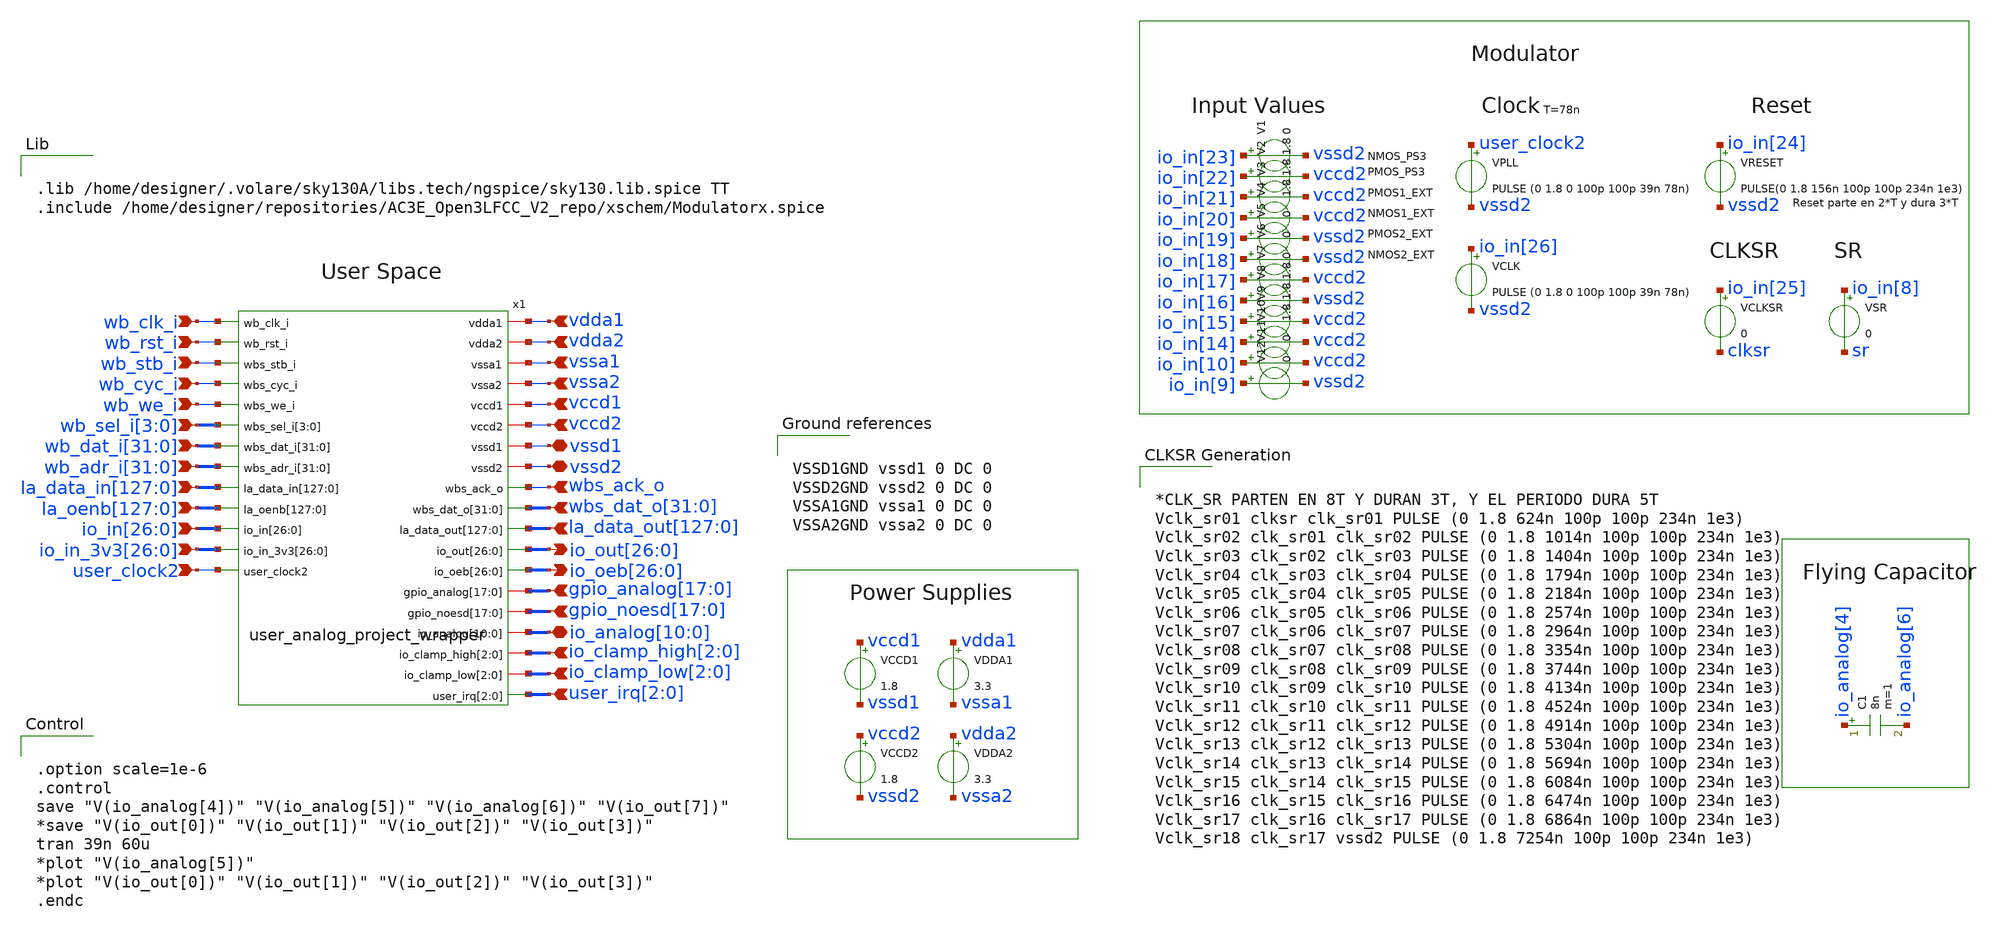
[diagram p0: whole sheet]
** sch_path: xschem/tb_top.sch
**.subckt tb_top vdda1 vdda2 vssa1 vssa2 vccd1 vccd2 vssd1 vssd2 wbs_ack_o
*+ wbs_dat_o[31],wbs_dat_o[30],wbs_dat_o[29],wbs_dat_o[28],wbs_dat_o[27],wbs_dat_o[26],wbs_dat_o[25],wbs_dat_o[24],wbs_dat_o[23],wbs_dat_o[22],wbs_dat_o[21],wbs_dat_o[20],wbs_dat_o[19],wbs_dat_o[18],wbs_dat_o[17],wbs_dat_o[16],wbs_dat_o[15],wbs_dat_o[14],wbs_dat_o[13],wbs_dat_o[12],wbs_dat_o[11],wbs_dat_o[10],wbs_dat_o[9],wbs_dat_o[8],wbs_dat_o[7],wbs_dat_o[6],wbs_dat_o[5],wbs_dat_o[4],wbs_dat_o[3],wbs_dat_o[2],wbs_dat_o[1],wbs_dat_o[0]
*+ la_data_out[127],la_data_out[126],la_data_out[125],la_data_out[124],la_data_out[123],la_data_out[122],la_data_out[121],la_data_out[120],la_data_out[119],la_data_out[118],la_data_out[117],la_data_out[116],la_data_out[115],la_data_out[114],la_data_out[113],la_data_out[112],la_data_out[111],la_data_out[110],la_data_out[109],la_data_out[108],la_data_out[107],la_data_out[106],la_data_out[105],la_data_out[104],la_data_out[103],la_data_out[102],la_data_out[101],la_data_out[100],la_data_out[99],la_data_out[98],la_data_out[97],la_data_out[96],la_data_out[95],la_data_out[94],la_data_out[93],la_data_out[92],la_data_out[91],la_data_out[90],la_data_out[89],la_data_out[88],la_data_out[87],la_data_out[86],la_data_out[85],la_data_out[84],la_data_out[83],la_data_out[82],la_data_out[81],la_data_out[80],la_data_out[79],la_data_out[78],la_data_out[77],la_data_out[76],la_data_out[75],la_data_out[74],la_data_out[73],la_data_out[72],la_data_out[71],la_data_out[70],la_data_out[69],la_data_out[68],la_data_out[67],la_data_out[66],la_data_out[65],la_data_out[64],la_data_out[63],la_data_out[62],la_data_out[61],la_data_out[60],la_data_out[59],la_data_out[58],la_data_out[57],la_data_out[56],la_data_out[55],la_data_out[54],la_data_out[53],la_data_out[52],la_data_out[51],la_data_out[50],la_data_out[49],la_data_out[48],la_data_out[47],la_data_out[46],la_data_out[45],la_data_out[44],la_data_out[43],la_data_out[42],la_data_out[41],la_data_out[40],la_data_out[39],la_data_out[38],la_data_out[37],la_data_out[36],la_data_out[35],la_data_out[34],la_data_out[33],la_data_out[32],la_data_out[31],la_data_out[30],la_data_out[29],la_data_out[28],la_data_out[27],la_data_out[26],la_data_out[25],la_data_out[24],la_data_out[23],la_data_out[22],la_data_out[21],la_data_out[20],la_data_out[19],la_data_out[18],la_data_out[17],la_data_out[16],la_data_out[15],la_data_out[14],la_data_out[13],la_data_out[12],la_data_out[11],la_data_out[10],la_data_out[9],la_data_out[8],la_data_out[7],la_data_out[6],la_data_out[5],la_data_out[4],la_data_out[3],la_data_out[2],la_data_out[1],la_data_out[0]
*+ io_out[26],io_out[25],io_out[24],io_out[23],io_out[22],io_out[21],io_out[20],io_out[19],io_out[18],io_out[17],io_out[16],io_out[15],io_out[14],io_out[13],io_out[12],io_out[11],io_out[10],io_out[9],io_out[8],io_out[7],io_out[6],io_out[5],io_out[4],io_out[3],io_out[2],io_out[1],io_out[0]
*+ io_oeb[26],io_oeb[25],io_oeb[24],io_oeb[23],io_oeb[22],io_oeb[21],io_oeb[20],io_oeb[19],io_oeb[18],io_oeb[17],io_oeb[16],io_oeb[15],io_oeb[14],io_oeb[13],io_oeb[12],io_oeb[11],io_oeb[10],io_oeb[9],io_oeb[8],io_oeb[7],io_oeb[6],io_oeb[5],io_oeb[4],io_oeb[3],io_oeb[2],io_oeb[1],io_oeb[0]
*+ gpio_analog[17],gpio_analog[16],gpio_analog[15],gpio_analog[14],gpio_analog[13],gpio_analog[12],gpio_analog[11],gpio_analog[10],gpio_analog[9],gpio_analog[8],gpio_analog[7],gpio_analog[6],gpio_analog[5],gpio_analog[4],gpio_analog[3],gpio_analog[2],gpio_analog[1],gpio_analog[0]
*+ gpio_noesd[17],gpio_noesd[16],gpio_noesd[15],gpio_noesd[14],gpio_noesd[13],gpio_noesd[12],gpio_noesd[11],gpio_noesd[10],gpio_noesd[9],gpio_noesd[8],gpio_noesd[7],gpio_noesd[6],gpio_noesd[5],gpio_noesd[4],gpio_noesd[3],gpio_noesd[2],gpio_noesd[1],gpio_noesd[0]
*+ io_analog[10],io_analog[9],io_analog[8],io_analog[7],io_analog[6],io_analog[5],io_analog[4],io_analog[3],io_analog[2],io_analog[1],io_analog[0] io_clamp_high[2],io_clamp_high[1],io_clamp_high[0] io_clamp_low[2],io_clamp_low[1],io_clamp_low[0]
*+ user_irq[2],user_irq[1],user_irq[0] wb_clk_i wb_rst_i wb_stb_i wb_cyc_i wb_we_i wb_sel_i[3],wb_sel_i[2],wb_sel_i[1],wb_sel_i[0]
*+ wb_dat_i[31],wb_dat_i[30],wb_dat_i[29],wb_dat_i[28],wb_dat_i[27],wb_dat_i[26],wb_dat_i[25],wb_dat_i[24],wb_dat_i[23],wb_dat_i[22],wb_dat_i[21],wb_dat_i[20],wb_dat_i[19],wb_dat_i[18],wb_dat_i[17],wb_dat_i[16],wb_dat_i[15],wb_dat_i[14],wb_dat_i[13],wb_dat_i[12],wb_dat_i[11],wb_dat_i[10],wb_dat_i[9],wb_dat_i[8],wb_dat_i[7],wb_dat_i[6],wb_dat_i[5],wb_dat_i[4],wb_dat_i[3],wb_dat_i[2],wb_dat_i[1],wb_dat_i[0]
*+ wb_adr_i[31],wb_adr_i[30],wb_adr_i[29],wb_adr_i[28],wb_adr_i[27],wb_adr_i[26],wb_adr_i[25],wb_adr_i[24],wb_adr_i[23],wb_adr_i[22],wb_adr_i[21],wb_adr_i[20],wb_adr_i[19],wb_adr_i[18],wb_adr_i[17],wb_adr_i[16],wb_adr_i[15],wb_adr_i[14],wb_adr_i[13],wb_adr_i[12],wb_adr_i[11],wb_adr_i[10],wb_adr_i[9],wb_adr_i[8],wb_adr_i[7],wb_adr_i[6],wb_adr_i[5],wb_adr_i[4],wb_adr_i[3],wb_adr_i[2],wb_adr_i[1],wb_adr_i[0]
*+ la_data_in[127],la_data_in[126],la_data_in[125],la_data_in[124],la_data_in[123],la_data_in[122],la_data_in[121],la_data_in[120],la_data_in[119],la_data_in[118],la_data_in[117],la_data_in[116],la_data_in[115],la_data_in[114],la_data_in[113],la_data_in[112],la_data_in[111],la_data_in[110],la_data_in[109],la_data_in[108],la_data_in[107],la_data_in[106],la_data_in[105],la_data_in[104],la_data_in[103],la_data_in[102],la_data_in[101],la_data_in[100],la_data_in[99],la_data_in[98],la_data_in[97],la_data_in[96],la_data_in[95],la_data_in[94],la_data_in[93],la_data_in[92],la_data_in[91],la_data_in[90],la_data_in[89],la_data_in[88],la_data_in[87],la_data_in[86],la_data_in[85],la_data_in[84],la_data_in[83],la_data_in[82],la_data_in[81],la_data_in[80],la_data_in[79],la_data_in[78],la_data_in[77],la_data_in[76],la_data_in[75],la_data_in[74],la_data_in[73],la_data_in[72],la_data_in[71],la_data_in[70],la_data_in[69],la_data_in[68],la_data_in[67],la_data_in[66],la_data_in[65],la_data_in[64],la_data_in[63],la_data_in[62],la_data_in[61],la_data_in[60],la_data_in[59],la_data_in[58],la_data_in[57],la_data_in[56],la_data_in[55],la_data_in[54],la_data_in[53],la_data_in[52],la_data_in[51],la_data_in[50],la_data_in[49],la_data_in[48],la_data_in[47],la_data_in[46],la_data_in[45],la_data_in[44],la_data_in[43],la_data_in[42],la_data_in[41],la_data_in[40],la_data_in[39],la_data_in[38],la_data_in[37],la_data_in[36],la_data_in[35],la_data_in[34],la_data_in[33],la_data_in[32],la_data_in[31],la_data_in[30],la_data_in[29],la_data_in[28],la_data_in[27],la_data_in[26],la_data_in[25],la_data_in[24],la_data_in[23],la_data_in[22],la_data_in[21],la_data_in[20],la_data_in[19],la_data_in[18],la_data_in[17],la_data_in[16],la_data_in[15],la_data_in[14],la_data_in[13],la_data_in[12],la_data_in[11],la_data_in[10],la_data_in[9],la_data_in[8],la_data_in[7],la_data_in[6],la_data_in[5],la_data_in[4],la_data_in[3],la_data_in[2],la_data_in[1],la_data_in[0]
*+ la_oenb[127],la_oenb[126],la_oenb[125],la_oenb[124],la_oenb[123],la_oenb[122],la_oenb[121],la_oenb[120],la_oenb[119],la_oenb[118],la_oenb[117],la_oenb[116],la_oenb[115],la_oenb[114],la_oenb[113],la_oenb[112],la_oenb[111],la_oenb[110],la_oenb[109],la_oenb[108],la_oenb[107],la_oenb[106],la_oenb[105],la_oenb[104],la_oenb[103],la_oenb[102],la_oenb[101],la_oenb[100],la_oenb[99],la_oenb[98],la_oenb[97],la_oenb[96],la_oenb[95],la_oenb[94],la_oenb[93],la_oenb[92],la_oenb[91],la_oenb[90],la_oenb[89],la_oenb[88],la_oenb[87],la_oenb[86],la_oenb[85],la_oenb[84],la_oenb[83],la_oenb[82],la_oenb[81],la_oenb[80],la_oenb[79],la_oenb[78],la_oenb[77],la_oenb[76],la_oenb[75],la_oenb[74],la_oenb[73],la_oenb[72],la_oenb[71],la_oenb[70],la_oenb[69],la_oenb[68],la_oenb[67],la_oenb[66],la_oenb[65],la_oenb[64],la_oenb[63],la_oenb[62],la_oenb[61],la_oenb[60],la_oenb[59],la_oenb[58],la_oenb[57],la_oenb[56],la_oenb[55],la_oenb[54],la_oenb[53],la_oenb[52],la_oenb[51],la_oenb[50],la_oenb[49],la_oenb[48],la_oenb[47],la_oenb[46],la_oenb[45],la_oenb[44],la_oenb[43],la_oenb[42],la_oenb[41],la_oenb[40],la_oenb[39],la_oenb[38],la_oenb[37],la_oenb[36],la_oenb[35],la_oenb[34],la_oenb[33],la_oenb[32],la_oenb[31],la_oenb[30],la_oenb[29],la_oenb[28],la_oenb[27],la_oenb[26],la_oenb[25],la_oenb[24],la_oenb[23],la_oenb[22],la_oenb[21],la_oenb[20],la_oenb[19],la_oenb[18],la_oenb[17],la_oenb[16],la_oenb[15],la_oenb[14],la_oenb[13],la_oenb[12],la_oenb[11],la_oenb[10],la_oenb[9],la_oenb[8],la_oenb[7],la_oenb[6],la_oenb[5],la_oenb[4],la_oenb[3],la_oenb[2],la_oenb[1],la_oenb[0]
*+ io_in[26],io_in[25],io_in[24],io_in[23],io_in[22],io_in[21],io_in[20],io_in[19],io_in[18],io_in[17],io_in[16],io_in[15],io_in[14],io_in[13],io_in[12],io_in[11],io_in[10],io_in[9],io_in[8],io_in[7],io_in[6],io_in[5],io_in[4],io_in[3],io_in[2],io_in[1],io_in[0]
*+ io_in_3v3[26],io_in_3v3[25],io_in_3v3[24],io_in_3v3[23],io_in_3v3[22],io_in_3v3[21],io_in_3v3[20],io_in_3v3[19],io_in_3v3[18],io_in_3v3[17],io_in_3v3[16],io_in_3v3[15],io_in_3v3[14],io_in_3v3[13],io_in_3v3[12],io_in_3v3[11],io_in_3v3[10],io_in_3v3[9],io_in_3v3[8],io_in_3v3[7],io_in_3v3[6],io_in_3v3[5],io_in_3v3[4],io_in_3v3[3],io_in_3v3[2],io_in_3v3[1],io_in_3v3[0] user_clock2
*.ipin vdda1
*.ipin vdda2
*.ipin vssa1
*.ipin vssa2
*.ipin vccd1
*.ipin vccd2
*.iopin vssd1
*.iopin vssd2
*.ipin wbs_ack_o
*.ipin
*+ wbs_dat_o[31],wbs_dat_o[30],wbs_dat_o[29],wbs_dat_o[28],wbs_dat_o[27],wbs_dat_o[26],wbs_dat_o[25],wbs_dat_o[24],wbs_dat_o[23],wbs_dat_o[22],wbs_dat_o[21],wbs_dat_o[20],wbs_dat_o[19],wbs_dat_o[18],wbs_dat_o[17],wbs_dat_o[16],wbs_dat_o[15],wbs_dat_o[14],wbs_dat_o[13],wbs_dat_o[12],wbs_dat_o[11],wbs_dat_o[10],wbs_dat_o[9],wbs_dat_o[8],wbs_dat_o[7],wbs_dat_o[6],wbs_dat_o[5],wbs_dat_o[4],wbs_dat_o[3],wbs_dat_o[2],wbs_dat_o[1],wbs_dat_o[0]
*.ipin
*+ la_data_out[127],la_data_out[126],la_data_out[125],la_data_out[124],la_data_out[123],la_data_out[122],la_data_out[121],la_data_out[120],la_data_out[119],la_data_out[118],la_data_out[117],la_data_out[116],la_data_out[115],la_data_out[114],la_data_out[113],la_data_out[112],la_data_out[111],la_data_out[110],la_data_out[109],la_data_out[108],la_data_out[107],la_data_out[106],la_data_out[105],la_data_out[104],la_data_out[103],la_data_out[102],la_data_out[101],la_data_out[100],la_data_out[99],la_data_out[98],la_data_out[97],la_data_out[96],la_data_out[95],la_data_out[94],la_data_out[93],la_data_out[92],la_data_out[91],la_data_out[90],la_data_out[89],la_data_out[88],la_data_out[87],la_data_out[86],la_data_out[85],la_data_out[84],la_data_out[83],la_data_out[82],la_data_out[81],la_data_out[80],la_data_out[79],la_data_out[78],la_data_out[77],la_data_out[76],la_data_out[75],la_data_out[74],la_data_out[73],la_data_out[72],la_data_out[71],la_data_out[70],la_data_out[69],la_data_out[68],la_data_out[67],la_data_out[66],la_data_out[65],la_data_out[64],la_data_out[63],la_data_out[62],la_data_out[61],la_data_out[60],la_data_out[59],la_data_out[58],la_data_out[57],la_data_out[56],la_data_out[55],la_data_out[54],la_data_out[53],la_data_out[52],la_data_out[51],la_data_out[50],la_data_out[49],la_data_out[48],la_data_out[47],la_data_out[46],la_data_out[45],la_data_out[44],la_data_out[43],la_data_out[42],la_data_out[41],la_data_out[40],la_data_out[39],la_data_out[38],la_data_out[37],la_data_out[36],la_data_out[35],la_data_out[34],la_data_out[33],la_data_out[32],la_data_out[31],la_data_out[30],la_data_out[29],la_data_out[28],la_data_out[27],la_data_out[26],la_data_out[25],la_data_out[24],la_data_out[23],la_data_out[22],la_data_out[21],la_data_out[20],la_data_out[19],la_data_out[18],la_data_out[17],la_data_out[16],la_data_out[15],la_data_out[14],la_data_out[13],la_data_out[12],la_data_out[11],la_data_out[10],la_data_out[9],la_data_out[8],la_data_out[7],la_data_out[6],la_data_out[5],la_data_out[4],la_data_out[3],la_data_out[2],la_data_out[1],la_data_out[0]
*.opin
*+ io_out[26],io_out[25],io_out[24],io_out[23],io_out[22],io_out[21],io_out[20],io_out[19],io_out[18],io_out[17],io_out[16],io_out[15],io_out[14],io_out[13],io_out[12],io_out[11],io_out[10],io_out[9],io_out[8],io_out[7],io_out[6],io_out[5],io_out[4],io_out[3],io_out[2],io_out[1],io_out[0]
*.opin
*+ io_oeb[26],io_oeb[25],io_oeb[24],io_oeb[23],io_oeb[22],io_oeb[21],io_oeb[20],io_oeb[19],io_oeb[18],io_oeb[17],io_oeb[16],io_oeb[15],io_oeb[14],io_oeb[13],io_oeb[12],io_oeb[11],io_oeb[10],io_oeb[9],io_oeb[8],io_oeb[7],io_oeb[6],io_oeb[5],io_oeb[4],io_oeb[3],io_oeb[2],io_oeb[1],io_oeb[0]
*.ipin
*+ gpio_analog[17],gpio_analog[16],gpio_analog[15],gpio_analog[14],gpio_analog[13],gpio_analog[12],gpio_analog[11],gpio_analog[10],gpio_analog[9],gpio_analog[8],gpio_analog[7],gpio_analog[6],gpio_analog[5],gpio_analog[4],gpio_analog[3],gpio_analog[2],gpio_analog[1],gpio_analog[0]
*.ipin
*+ gpio_noesd[17],gpio_noesd[16],gpio_noesd[15],gpio_noesd[14],gpio_noesd[13],gpio_noesd[12],gpio_noesd[11],gpio_noesd[10],gpio_noesd[9],gpio_noesd[8],gpio_noesd[7],gpio_noesd[6],gpio_noesd[5],gpio_noesd[4],gpio_noesd[3],gpio_noesd[2],gpio_noesd[1],gpio_noesd[0]
*.iopin
*+ io_analog[10],io_analog[9],io_analog[8],io_analog[7],io_analog[6],io_analog[5],io_analog[4],io_analog[3],io_analog[2],io_analog[1],io_analog[0]
*.ipin io_clamp_high[2],io_clamp_high[1],io_clamp_high[0]
*.ipin io_clamp_low[2],io_clamp_low[1],io_clamp_low[0]
*.ipin user_irq[2],user_irq[1],user_irq[0]
*.ipin wb_clk_i
*.ipin wb_rst_i
*.ipin wb_stb_i
*.ipin wb_cyc_i
*.ipin wb_we_i
*.ipin wb_sel_i[3],wb_sel_i[2],wb_sel_i[1],wb_sel_i[0]
*.ipin
*+ wb_dat_i[31],wb_dat_i[30],wb_dat_i[29],wb_dat_i[28],wb_dat_i[27],wb_dat_i[26],wb_dat_i[25],wb_dat_i[24],wb_dat_i[23],wb_dat_i[22],wb_dat_i[21],wb_dat_i[20],wb_dat_i[19],wb_dat_i[18],wb_dat_i[17],wb_dat_i[16],wb_dat_i[15],wb_dat_i[14],wb_dat_i[13],wb_dat_i[12],wb_dat_i[11],wb_dat_i[10],wb_dat_i[9],wb_dat_i[8],wb_dat_i[7],wb_dat_i[6],wb_dat_i[5],wb_dat_i[4],wb_dat_i[3],wb_dat_i[2],wb_dat_i[1],wb_dat_i[0]
*.ipin
*+ wb_adr_i[31],wb_adr_i[30],wb_adr_i[29],wb_adr_i[28],wb_adr_i[27],wb_adr_i[26],wb_adr_i[25],wb_adr_i[24],wb_adr_i[23],wb_adr_i[22],wb_adr_i[21],wb_adr_i[20],wb_adr_i[19],wb_adr_i[18],wb_adr_i[17],wb_adr_i[16],wb_adr_i[15],wb_adr_i[14],wb_adr_i[13],wb_adr_i[12],wb_adr_i[11],wb_adr_i[10],wb_adr_i[9],wb_adr_i[8],wb_adr_i[7],wb_adr_i[6],wb_adr_i[5],wb_adr_i[4],wb_adr_i[3],wb_adr_i[2],wb_adr_i[1],wb_adr_i[0]
*.ipin
*+ la_data_in[127],la_data_in[126],la_data_in[125],la_data_in[124],la_data_in[123],la_data_in[122],la_data_in[121],la_data_in[120],la_data_in[119],la_data_in[118],la_data_in[117],la_data_in[116],la_data_in[115],la_data_in[114],la_data_in[113],la_data_in[112],la_data_in[111],la_data_in[110],la_data_in[109],la_data_in[108],la_data_in[107],la_data_in[106],la_data_in[105],la_data_in[104],la_data_in[103],la_data_in[102],la_data_in[101],la_data_in[100],la_data_in[99],la_data_in[98],la_data_in[97],la_data_in[96],la_data_in[95],la_data_in[94],la_data_in[93],la_data_in[92],la_data_in[91],la_data_in[90],la_data_in[89],la_data_in[88],la_data_in[87],la_data_in[86],la_data_in[85],la_data_in[84],la_data_in[83],la_data_in[82],la_data_in[81],la_data_in[80],la_data_in[79],la_data_in[78],la_data_in[77],la_data_in[76],la_data_in[75],la_data_in[74],la_data_in[73],la_data_in[72],la_data_in[71],la_data_in[70],la_data_in[69],la_data_in[68],la_data_in[67],la_data_in[66],la_data_in[65],la_data_in[64],la_data_in[63],la_data_in[62],la_data_in[61],la_data_in[60],la_data_in[59],la_data_in[58],la_data_in[57],la_data_in[56],la_data_in[55],la_data_in[54],la_data_in[53],la_data_in[52],la_data_in[51],la_data_in[50],la_data_in[49],la_data_in[48],la_data_in[47],la_data_in[46],la_data_in[45],la_data_in[44],la_data_in[43],la_data_in[42],la_data_in[41],la_data_in[40],la_data_in[39],la_data_in[38],la_data_in[37],la_data_in[36],la_data_in[35],la_data_in[34],la_data_in[33],la_data_in[32],la_data_in[31],la_data_in[30],la_data_in[29],la_data_in[28],la_data_in[27],la_data_in[26],la_data_in[25],la_data_in[24],la_data_in[23],la_data_in[22],la_data_in[21],la_data_in[20],la_data_in[19],la_data_in[18],la_data_in[17],la_data_in[16],la_data_in[15],la_data_in[14],la_data_in[13],la_data_in[12],la_data_in[11],la_data_in[10],la_data_in[9],la_data_in[8],la_data_in[7],la_data_in[6],la_data_in[5],la_data_in[4],la_data_in[3],la_data_in[2],la_data_in[1],la_data_in[0]
*.ipin
*+ la_oenb[127],la_oenb[126],la_oenb[125],la_oenb[124],la_oenb[123],la_oenb[122],la_oenb[121],la_oenb[120],la_oenb[119],la_oenb[118],la_oenb[117],la_oenb[116],la_oenb[115],la_oenb[114],la_oenb[113],la_oenb[112],la_oenb[111],la_oenb[110],la_oenb[109],la_oenb[108],la_oenb[107],la_oenb[106],la_oenb[105],la_oenb[104],la_oenb[103],la_oenb[102],la_oenb[101],la_oenb[100],la_oenb[99],la_oenb[98],la_oenb[97],la_oenb[96],la_oenb[95],la_oenb[94],la_oenb[93],la_oenb[92],la_oenb[91],la_oenb[90],la_oenb[89],la_oenb[88],la_oenb[87],la_oenb[86],la_oenb[85],la_oenb[84],la_oenb[83],la_oenb[82],la_oenb[81],la_oenb[80],la_oenb[79],la_oenb[78],la_oenb[77],la_oenb[76],la_oenb[75],la_oenb[74],la_oenb[73],la_oenb[72],la_oenb[71],la_oenb[70],la_oenb[69],la_oenb[68],la_oenb[67],la_oenb[66],la_oenb[65],la_oenb[64],la_oenb[63],la_oenb[62],la_oenb[61],la_oenb[60],la_oenb[59],la_oenb[58],la_oenb[57],la_oenb[56],la_oenb[55],la_oenb[54],la_oenb[53],la_oenb[52],la_oenb[51],la_oenb[50],la_oenb[49],la_oenb[48],la_oenb[47],la_oenb[46],la_oenb[45],la_oenb[44],la_oenb[43],la_oenb[42],la_oenb[41],la_oenb[40],la_oenb[39],la_oenb[38],la_oenb[37],la_oenb[36],la_oenb[35],la_oenb[34],la_oenb[33],la_oenb[32],la_oenb[31],la_oenb[30],la_oenb[29],la_oenb[28],la_oenb[27],la_oenb[26],la_oenb[25],la_oenb[24],la_oenb[23],la_oenb[22],la_oenb[21],la_oenb[20],la_oenb[19],la_oenb[18],la_oenb[17],la_oenb[16],la_oenb[15],la_oenb[14],la_oenb[13],la_oenb[12],la_oenb[11],la_oenb[10],la_oenb[9],la_oenb[8],la_oenb[7],la_oenb[6],la_oenb[5],la_oenb[4],la_oenb[3],la_oenb[2],la_oenb[1],la_oenb[0]
*.ipin
*+ io_in[26],io_in[25],io_in[24],io_in[23],io_in[22],io_in[21],io_in[20],io_in[19],io_in[18],io_in[17],io_in[16],io_in[15],io_in[14],io_in[13],io_in[12],io_in[11],io_in[10],io_in[9],io_in[8],io_in[7],io_in[6],io_in[5],io_in[4],io_in[3],io_in[2],io_in[1],io_in[0]
*.ipin
*+ io_in_3v3[26],io_in_3v3[25],io_in_3v3[24],io_in_3v3[23],io_in_3v3[22],io_in_3v3[21],io_in_3v3[20],io_in_3v3[19],io_in_3v3[18],io_in_3v3[17],io_in_3v3[16],io_in_3v3[15],io_in_3v3[14],io_in_3v3[13],io_in_3v3[12],io_in_3v3[11],io_in_3v3[10],io_in_3v3[9],io_in_3v3[8],io_in_3v3[7],io_in_3v3[6],io_in_3v3[5],io_in_3v3[4],io_in_3v3[3],io_in_3v3[2],io_in_3v3[1],io_in_3v3[0]
*.ipin user_clock2
x1 vdda1 vdda2 vssa1 vssa2 vccd1 vccd2 vssd1 vssd2 wb_clk_i wb_rst_i wb_stb_i wb_cyc_i wb_we_i
+ wb_sel_i[3] wb_sel_i[2] wb_sel_i[1] wb_sel_i[0] wb_dat_i[31] wb_dat_i[30] wb_dat_i[29] wb_dat_i[28]
+ wb_dat_i[27] wb_dat_i[26] wb_dat_i[25] wb_dat_i[24] wb_dat_i[23] wb_dat_i[22] wb_dat_i[21] wb_dat_i[20]
+ wb_dat_i[19] wb_dat_i[18] wb_dat_i[17] wb_dat_i[16] wb_dat_i[15] wb_dat_i[14] wb_dat_i[13] wb_dat_i[12]
+ wb_dat_i[11] wb_dat_i[10] wb_dat_i[9] wb_dat_i[8] wb_dat_i[7] wb_dat_i[6] wb_dat_i[5] wb_dat_i[4] wb_dat_i[3]
+ wb_dat_i[2] wb_dat_i[1] wb_dat_i[0] wb_adr_i[31] wb_adr_i[30] wb_adr_i[29] wb_adr_i[28] wb_adr_i[27]
+ wb_adr_i[26] wb_adr_i[25] wb_adr_i[24] wb_adr_i[23] wb_adr_i[22] wb_adr_i[21] wb_adr_i[20] wb_adr_i[19]
+ wb_adr_i[18] wb_adr_i[17] wb_adr_i[16] wb_adr_i[15] wb_adr_i[14] wb_adr_i[13] wb_adr_i[12] wb_adr_i[11]
+ wb_adr_i[10] wb_adr_i[9] wb_adr_i[8] wb_adr_i[7] wb_adr_i[6] wb_adr_i[5] wb_adr_i[4] wb_adr_i[3] wb_adr_i[2]
+ wb_adr_i[1] wb_adr_i[0] wbs_ack_o wbs_dat_o[31] wbs_dat_o[30] wbs_dat_o[29] wbs_dat_o[28] wbs_dat_o[27]
+ wbs_dat_o[26] wbs_dat_o[25] wbs_dat_o[24] wbs_dat_o[23] wbs_dat_o[22] wbs_dat_o[21] wbs_dat_o[20] wbs_dat_o[19]
+ wbs_dat_o[18] wbs_dat_o[17] wbs_dat_o[16] wbs_dat_o[15] wbs_dat_o[14] wbs_dat_o[13] wbs_dat_o[12] wbs_dat_o[11]
+ wbs_dat_o[10] wbs_dat_o[9] wbs_dat_o[8] wbs_dat_o[7] wbs_dat_o[6] wbs_dat_o[5] wbs_dat_o[4] wbs_dat_o[3]
+ wbs_dat_o[2] wbs_dat_o[1] wbs_dat_o[0] la_data_in[127] la_data_in[126] la_data_in[125] la_data_in[124]
+ la_data_in[123] la_data_in[122] la_data_in[121] la_data_in[120] la_data_in[119] la_data_in[118] la_data_in[117]
+ la_data_in[116] la_data_in[115] la_data_in[114] la_data_in[113] la_data_in[112] la_data_in[111] la_data_in[110]
+ la_data_in[109] la_data_in[108] la_data_in[107] la_data_in[106] la_data_in[105] la_data_in[104] la_data_in[103]
+ la_data_in[102] la_data_in[101] la_data_in[100] la_data_in[99] la_data_in[98] la_data_in[97] la_data_in[96]
+ la_data_in[95] la_data_in[94] la_data_in[93] la_data_in[92] la_data_in[91] la_data_in[90] la_data_in[89]
+ la_data_in[88] la_data_in[87] la_data_in[86] la_data_in[85] la_data_in[84] la_data_in[83] la_data_in[82]
+ la_data_in[81] la_data_in[80] la_data_in[79] la_data_in[78] la_data_in[77] la_data_in[76] la_data_in[75]
+ la_data_in[74] la_data_in[73] la_data_in[72] la_data_in[71] la_data_in[70] la_data_in[69] la_data_in[68]
+ la_data_in[67] la_data_in[66] la_data_in[65] la_data_in[64] la_data_in[63] la_data_in[62] la_data_in[61]
+ la_data_in[60] la_data_in[59] la_data_in[58] la_data_in[57] la_data_in[56] la_data_in[55] la_data_in[54]
+ la_data_in[53] la_data_in[52] la_data_in[51] la_data_in[50] la_data_in[49] la_data_in[48] la_data_in[47]
+ la_data_in[46] la_data_in[45] la_data_in[44] la_data_in[43] la_data_in[42] la_data_in[41] la_data_in[40]
+ la_data_in[39] la_data_in[38] la_data_in[37] la_data_in[36] la_data_in[35] la_data_in[34] la_data_in[33]
+ la_data_in[32] la_data_in[31] la_data_in[30] la_data_in[29] la_data_in[28] la_data_in[27] la_data_in[26]
+ la_data_in[25] la_data_in[24] la_data_in[23] la_data_in[22] la_data_in[21] la_data_in[20] la_data_in[19]
+ la_data_in[18] la_data_in[17] la_data_in[16] la_data_in[15] la_data_in[14] la_data_in[13] la_data_in[12]
+ la_data_in[11] la_data_in[10] la_data_in[9] la_data_in[8] la_data_in[7] la_data_in[6] la_data_in[5] la_data_in[4]
+ la_data_in[3] la_data_in[2] la_data_in[1] la_data_in[0] la_data_out[127] la_data_out[126] la_data_out[125]
+ la_data_out[124] la_data_out[123] la_data_out[122] la_data_out[121] la_data_out[120] la_data_out[119]
+ la_data_out[118] la_data_out[117] la_data_out[116] la_data_out[115] la_data_out[114] la_data_out[113]
+ la_data_out[112] la_data_out[111] la_data_out[110] la_data_out[109] la_data_out[108] la_data_out[107]
+ la_data_out[106] la_data_out[105] la_data_out[104] la_data_out[103] la_data_out[102] la_data_out[101]
+ la_data_out[100] la_data_out[99] la_data_out[98] la_data_out[97] la_data_out[96] la_data_out[95] la_data_out[94]
+ la_data_out[93] la_data_out[92] la_data_out[91] la_data_out[90] la_data_out[89] la_data_out[88] la_data_out[87]
+ la_data_out[86] la_data_out[85] la_data_out[84] la_data_out[83] la_data_out[82] la_data_out[81] la_data_out[80]
+ la_data_out[79] la_data_out[78] la_data_out[77] la_data_out[76] la_data_out[75] la_data_out[74] la_data_out[73]
+ la_data_out[72] la_data_out[71] la_data_out[70] la_data_out[69] la_data_out[68] la_data_out[67] la_data_out[66]
+ la_data_out[65] la_data_out[64] la_data_out[63] la_data_out[62] la_data_out[61] la_data_out[60] la_data_out[59]
+ la_data_out[58] la_data_out[57] la_data_out[56] la_data_out[55] la_data_out[54] la_data_out[53] la_data_out[52]
+ la_data_out[51] la_data_out[50] la_data_out[49] la_data_out[48] la_data_out[47] la_data_out[46] la_data_out[45]
+ la_data_out[44] la_data_out[43] la_data_out[42] la_data_out[41] la_data_out[40] la_data_out[39] la_data_out[38]
+ la_data_out[37] la_data_out[36] la_data_out[35] la_data_out[34] la_data_out[33] la_data_out[32] la_data_out[31]
+ la_data_out[30] la_data_out[29] la_data_out[28] la_data_out[27] la_data_out[26] la_data_out[25] la_data_out[24]
+ la_data_out[23] la_data_out[22] la_data_out[21] la_data_out[20] la_data_out[19] la_data_out[18] la_data_out[17]
+ la_data_out[16] la_data_out[15] la_data_out[14] la_data_out[13] la_data_out[12] la_data_out[11] la_data_out[10]
+ la_data_out[9] la_data_out[8] la_data_out[7] la_data_out[6] la_data_out[5] la_data_out[4] la_data_out[3]
+ la_data_out[2] la_data_out[1] la_data_out[0] la_oenb[127] la_oenb[126] la_oenb[125] la_oenb[124] la_oenb[123]
+ la_oenb[122] la_oenb[121] la_oenb[120] la_oenb[119] la_oenb[118] la_oenb[117] la_oenb[116] la_oenb[115]
+ la_oenb[114] la_oenb[113] la_oenb[112] la_oenb[111] la_oenb[110] la_oenb[109] la_oenb[108] la_oenb[107]
+ la_oenb[106] la_oenb[105] la_oenb[104] la_oenb[103] la_oenb[102] la_oenb[101] la_oenb[100] la_oenb[99]
+ la_oenb[98] la_oenb[97] la_oenb[96] la_oenb[95] la_oenb[94] la_oenb[93] la_oenb[92] la_oenb[91] la_oenb[90]
+ la_oenb[89] la_oenb[88] la_oenb[87] la_oenb[86] la_oenb[85] la_oenb[84] la_oenb[83] la_oenb[82] la_oenb[81]
+ la_oenb[80] la_oenb[79] la_oenb[78] la_oenb[77] la_oenb[76] la_oenb[75] la_oenb[74] la_oenb[73] la_oenb[72]
+ la_oenb[71] la_oenb[70] la_oenb[69] la_oenb[68] la_oenb[67] la_oenb[66] la_oenb[65] la_oenb[64] la_oenb[63]
+ la_oenb[62] la_oenb[61] la_oenb[60] la_oenb[59] la_oenb[58] la_oenb[57] la_oenb[56] la_oenb[55] la_oenb[54]
+ la_oenb[53] la_oenb[52] la_oenb[51] la_oenb[50] la_oenb[49] la_oenb[48] la_oenb[47] la_oenb[46] la_oenb[45]
+ la_oenb[44] la_oenb[43] la_oenb[42] la_oenb[41] la_oenb[40] la_oenb[39] la_oenb[38] la_oenb[37] la_oenb[36]
+ la_oenb[35] la_oenb[34] la_oenb[33] la_oenb[32] la_oenb[31] la_oenb[30] la_oenb[29] la_oenb[28] la_oenb[27]
+ la_oenb[26] la_oenb[25] la_oenb[24] la_oenb[23] la_oenb[22] la_oenb[21] la_oenb[20] la_oenb[19] la_oenb[18]
+ la_oenb[17] la_oenb[16] la_oenb[15] la_oenb[14] la_oenb[13] la_oenb[12] la_oenb[11] la_oenb[10] la_oenb[9]
+ la_oenb[8] la_oenb[7] la_oenb[6] la_oenb[5] la_oenb[4] la_oenb[3] la_oenb[2] la_oenb[1] la_oenb[0] io_in[26]
+ io_in[25] io_in[24] io_in[23] io_in[22] io_in[21] io_in[20] io_in[19] io_in[18] io_in[17] io_in[16] io_in[15]
+ io_in[14] io_in[13] io_in[12] io_in[11] io_in[10] io_in[9] io_in[8] io_in[7] io_in[6] io_in[5] io_in[4]
+ io_in[3] io_in[2] io_in[1] io_in[0] io_in_3v3[26] io_in_3v3[25] io_in_3v3[24] io_in_3v3[23] io_in_3v3[22]
+ io_in_3v3[21] io_in_3v3[20] io_in_3v3[19] io_in_3v3[18] io_in_3v3[17] io_in_3v3[16] io_in_3v3[15] io_in_3v3[14]
+ io_in_3v3[13] io_in_3v3[12] io_in_3v3[11] io_in_3v3[10] io_in_3v3[9] io_in_3v3[8] io_in_3v3[7] io_in_3v3[6]
+ io_in_3v3[5] io_in_3v3[4] io_in_3v3[3] io_in_3v3[2] io_in_3v3[1] io_in_3v3[0] io_out[26] io_out[25] io_out[24]
+ io_out[23] io_out[22] io_out[21] io_out[20] io_out[19] io_out[18] io_out[17] io_out[16] io_out[15] io_out[14]
+ io_out[13] io_out[12] io_out[11] io_out[10] io_out[9] io_out[8] io_out[7] io_out[6] io_out[5] io_out[4]
+ io_out[3] io_out[2] io_out[1] io_out[0] io_oeb[26] io_oeb[25] io_oeb[24] io_oeb[23] io_oeb[22] io_oeb[21]
+ io_oeb[20] io_oeb[19] io_oeb[18] io_oeb[17] io_oeb[16] io_oeb[15] io_oeb[14] io_oeb[13] io_oeb[12] io_oeb[11]
+ io_oeb[10] io_oeb[9] io_oeb[8] io_oeb[7] io_oeb[6] io_oeb[5] io_oeb[4] io_oeb[3] io_oeb[2] io_oeb[1] io_oeb[0]
+ gpio_analog[17] gpio_analog[16] gpio_analog[15] gpio_analog[14] gpio_analog[13] gpio_analog[12] gpio_analog[11]
+ gpio_analog[10] gpio_analog[9] gpio_analog[8] gpio_analog[7] gpio_analog[6] gpio_analog[5] gpio_analog[4]
+ gpio_analog[3] gpio_analog[2] gpio_analog[1] gpio_analog[0] gpio_noesd[17] gpio_noesd[16] gpio_noesd[15]
+ gpio_noesd[14] gpio_noesd[13] gpio_noesd[12] gpio_noesd[11] gpio_noesd[10] gpio_noesd[9] gpio_noesd[8]
+ gpio_noesd[7] gpio_noesd[6] gpio_noesd[5] gpio_noesd[4] gpio_noesd[3] gpio_noesd[2] gpio_noesd[1] gpio_noesd[0]
+ io_analog[10] io_analog[9] io_analog[8] io_analog[7] io_analog[6] io_analog[5] io_analog[4] io_analog[3]
+ io_analog[2] io_analog[1] io_analog[0] io_clamp_high[2] io_clamp_high[1] io_clamp_high[0] io_clamp_low[2]
+ io_clamp_low[1] io_clamp_low[0] user_clock2 user_irq[2] user_irq[1] user_irq[0] user_analog_project_wrapper
VCCD2 vccd2 vssd2 1.8
VPLL user_clock2 vssd2 PULSE (0 1.8 0 100p 100p 39n 78n)
VCLK io_in[26] vssd2 PULSE (0 1.8 0 100p 100p 39n 78n)
VRESET io_in[24] vssd2 PULSE(0 1.8 156n 100p 100p 234n 1e3)
V1 io_in[23] vssd2 0
V2 io_in[22] vccd2 1.8
V3 io_in[21] vccd2 1.8
V4 io_in[20] vccd2 1.8
V5 io_in[19] vssd2 0
V6 io_in[18] vssd2 0
V7 io_in[17] vccd2 0
V8 io_in[16] vssd2 1.8
V9 io_in[15] vccd2 1.8
V10 io_in[14] vccd2 1.8
V11 io_in[10] vccd2 0
V12 io_in[9] vssd2 0
VCCD1 vccd1 vssd1 1.8
VDDA1 vdda1 vssa1 3.3
VDDA2 vdda2 vssa2 3.3
C1 io_analog[4] io_analog[6] 8n m=1
VCLKSR io_in[25] clksr 0
VSR io_in[8] sr 0
**** begin user architecture code


.lib /home/designer/.volare/sky130A/libs.tech/ngspice/sky130.lib.spice TT
.include /home/designer/repositories/AC3E_Open3LFCC_V2_repo/xschem/Modulatorx.spice




.option scale=1e-6
.control
save "V(io_analog[4])" "V(io_analog[5])" "V(io_analog[6])" "V(io_out[7])"
*save "V(io_out[0])" "V(io_out[1])" "V(io_out[2])" "V(io_out[3])"
tran 39n 60u
*plot "V(io_analog[5])"
*plot "V(io_out[0])" "V(io_out[1])" "V(io_out[2])" "V(io_out[3])"
.endc




*CLK_SR PARTEN EN 8T Y DURAN 3T, Y EL PERIODO DURA 5T
Vclk_sr01 clksr clk_sr01 PULSE (0 1.8 624n 100p 100p 234n 1e3)
Vclk_sr02 clk_sr01 clk_sr02 PULSE (0 1.8 1014n 100p 100p 234n 1e3)
Vclk_sr03 clk_sr02 clk_sr03 PULSE (0 1.8 1404n 100p 100p 234n 1e3)
Vclk_sr04 clk_sr03 clk_sr04 PULSE (0 1.8 1794n 100p 100p 234n 1e3)
Vclk_sr05 clk_sr04 clk_sr05 PULSE (0 1.8 2184n 100p 100p 234n 1e3)
Vclk_sr06 clk_sr05 clk_sr06 PULSE (0 1.8 2574n 100p 100p 234n 1e3)
Vclk_sr07 clk_sr06 clk_sr07 PULSE (0 1.8 2964n 100p 100p 234n 1e3)
Vclk_sr08 clk_sr07 clk_sr08 PULSE (0 1.8 3354n 100p 100p 234n 1e3)
Vclk_sr09 clk_sr08 clk_sr09 PULSE (0 1.8 3744n 100p 100p 234n 1e3)
Vclk_sr10 clk_sr09 clk_sr10 PULSE (0 1.8 4134n 100p 100p 234n 1e3)
Vclk_sr11 clk_sr10 clk_sr11 PULSE (0 1.8 4524n 100p 100p 234n 1e3)
Vclk_sr12 clk_sr11 clk_sr12 PULSE (0 1.8 4914n 100p 100p 234n 1e3)
Vclk_sr13 clk_sr12 clk_sr13 PULSE (0 1.8 5304n 100p 100p 234n 1e3)
Vclk_sr14 clk_sr13 clk_sr14 PULSE (0 1.8 5694n 100p 100p 234n 1e3)
Vclk_sr15 clk_sr14 clk_sr15 PULSE (0 1.8 6084n 100p 100p 234n 1e3)
Vclk_sr16 clk_sr15 clk_sr16 PULSE (0 1.8 6474n 100p 100p 234n 1e3)
Vclk_sr17 clk_sr16 clk_sr17 PULSE (0 1.8 6864n 100p 100p 234n 1e3)
Vclk_sr18 clk_sr17 vssd2 PULSE (0 1.8 7254n 100p 100p 234n 1e3)





* Carga Shift register
*                     PULSE (de_voltaje a_voltaje parte_en 100p 100p dura 1e3)
* Data_SR (dt[0]) (1) parte en 7*T y dura 5*T
Vdata_sr01 sr sr01 PULSE (0 1.8 546n 100p 100p 389.8n 1e3)

* Data_SR (dt[1]) (1) parte en 12*T y dura 5*T
Vdata_sr02 sr01 sr02 PULSE (0 1.8 936n 100p 100p 390n 1e3)

* Data_SR (dt[2]) (0) parte en 17*T y dura 5*T
*Vdata_sr03 sr02 sr03 PULSE (0 1.8 1326n 100p 100p 390n 1e3)

* Data_SR (dt[3]) (0) parte en 22*P y dura 5*T
*Vdata_sr04 sr03 sr04 PULSE (0 1.8 1716n 100p 100p 390n 1e3)

* Data_SR (dt[4]) (0) parte en 27*T y dura 5*T
*Vdata_sr05 sr04 sr05 PULSE (0 1.8 2106n 100p 100p 390n 1e3)

* Data_SR (SELECTOR_SIGNAL_GENERATOR_1[0]) (0) parte en (7+5*5)T y dura 5*T
*Vdata_sr06 sr05 sr06 PULSE (0 1.8 2496n 100p 100p 390n 1e3)

* Data_SR (SELECTOR_SIGNAL_GENERATOR_1[1]) (0) parte (7+5*6)T y dura 5*T
*Vdata_sr07 sr06 sr07 PULSE (0 1.8 2886n 100p 100p 390n 1e3)

* Data_SR (SELECTOR_SIGNAL_GENERATOR_2[0]) (0) parte (7+5*7)T y dura 5*T
*Vdata_sr08 sr07 sr08 PULSE (0 1.8 3276n 100p 100p 390n 1e3)

* Data_SR (SELECTOR_SIGNAL_GENERATOR_2[2]) (1) parte (7+5*8)T y dura 5*T
Vdata_sr09 sr02 sr09 PULSE (0 1.8 3666n 100p 100p 390n 1e3)

* Data_SR (OUTPUT_SELECTOR_EXTERNAL[0]) (0) parte (7+5*9)T y dura 5*T
*Vdata_sr10 sr09 sr10 PULSE (0 1.8 4056n 100p 100p 390n 1e3)

* Data_SR (OUTPUT_SELECTOR_EXTERNAL[1]) (0) parte (7+5*10)T y dura 5*T
*Vdata_sr11 sr10 sr11 PULSE (0 1.8 4446n 100p 100p 390n 1e3)

* Data_SR (OUTPUT_SELECTOR_EXTERNAL[2]) (0) parte (7+5*11)T y dura 5*T
*Vdata_sr12 sr11 sr12 PULSE (0 1.8 4806n 100p 100p 390n 1e3)

* Data_SR (OUTPUT_SELECTOR_EXTERNAL[3]) (0) parte (7+5*12)T y dura 5*T
*Vdata_sr13 sr12 sr13 PULSE (0 1.8 5226n 100p 100p 390n 1e3)

* Data_SR (INPUT_SELECTOR) (0) parte (7+5*13)T y dura 5*T     **EN (1) PASAN LAS ENTRADAS DIRECTO A
*+ LAS SALIDAS**
*Vdata_sr14 sr09 sr14 PULSE (0 1.8 5616n 100p 100p 390n 1e3)

* Data_SR (CLK_SELECTOR) (0) parte en parte (7+5*14)T y dura 5*T    ** EN (1) USA EL CLK EXTERNO, EN
*+ (0) USA EL CLK DEL PLL**
*Vdata_sr15 sr14 sr15 PULSE (0 1.8 6006n 100p 100p 390n 1e3)

* Data_SR (PS_SELECTOR) (1) parte (7+5*15)T y dura 5*T   ** EN (1) LA SALIDA VA A PS1, EN (0) VA A
*+ PS2**
Vdata_sr16 sr09 sr16 PULSE (0 1.8 6396n 100p 100p 390n 1e3)

* Data_SR (PS3_SELECTOR) (0) parte (7+5*16)T y dura 5*T   ** EN (1) DEJA PASAR LAS SENALES d15 y d14
*+ DIRECTAMENTE A PS3 Y APAGA LAS SALIDAS A PS1 Y PS2, EN (0) FUNCIONA LA LOGICA DE PS_SELECTOR **
*Vdata_sr17 sr16 sr17 vssd2 PULSE (0 1.8 6786n 100p 100p 390n 1e3)

*Data_SR (ENABLE_OUTPUT) (1) parte (7+5*17)T y dura 5*T  ** EN (1) DEJA PASAR LA SALIDA CONFIGURADA,
*+ EN (0) LAS SALIDAS PROVOCAN QUE LOS TRANSISTORES ESTEN ABIERTOS**
Vdata_sr18 sr16 vssd2 PULSE (0 1.8 7176n 100p 100p 390n 1e3)





VSSD1GND vssd1 0 DC 0
VSSD2GND vssd2 0 DC 0
VSSA1GND vssa1 0 DC 0
VSSA2GND vssa2 0 DC 0


**** end user architecture code
**.ends
.end
